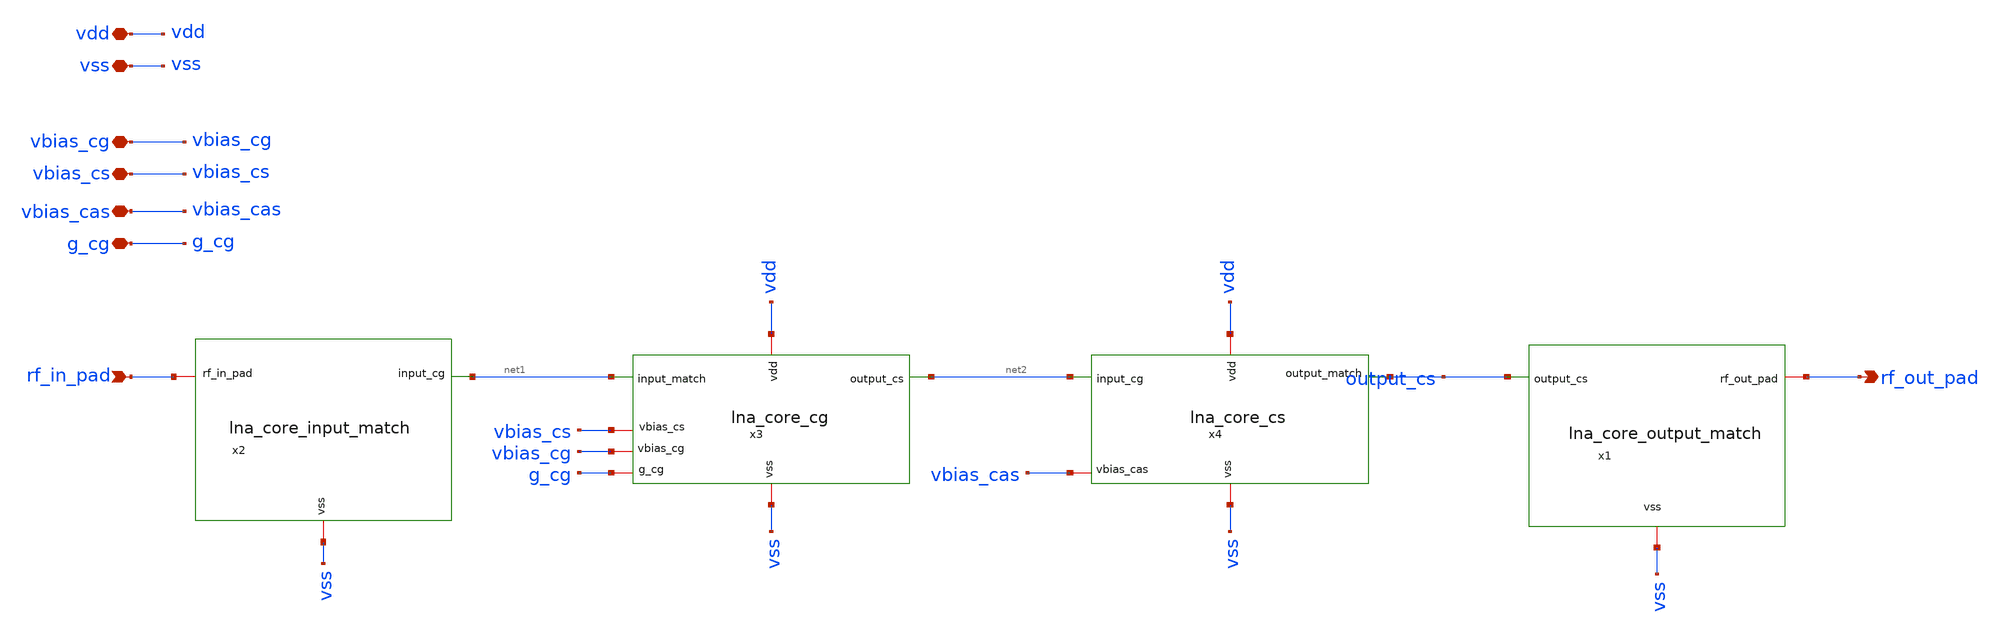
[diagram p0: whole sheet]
** sch_path: xschem/lna_core_parts.sch
**.subckt lna_core_parts rf_in_pad vbias_cg vbias_cs rf_out_pad vdd vss vbias_cas g_cg
*.ipin rf_in_pad
*.iopin vbias_cg
*.iopin vbias_cs
*.opin rf_out_pad
*.iopin vdd
*.iopin vss
*.iopin vbias_cas
*.iopin g_cg
x1 output_cs rf_out_pad vss lna_core_output_match
x2 vss net1 rf_in_pad lna_core_input_match
x3 vbias_cs vdd vss vbias_cg net2 g_cg net1 lna_core_cg
x4 output_cs vbias_cas net2 vdd vss lna_core_cs
**.ends
.end
